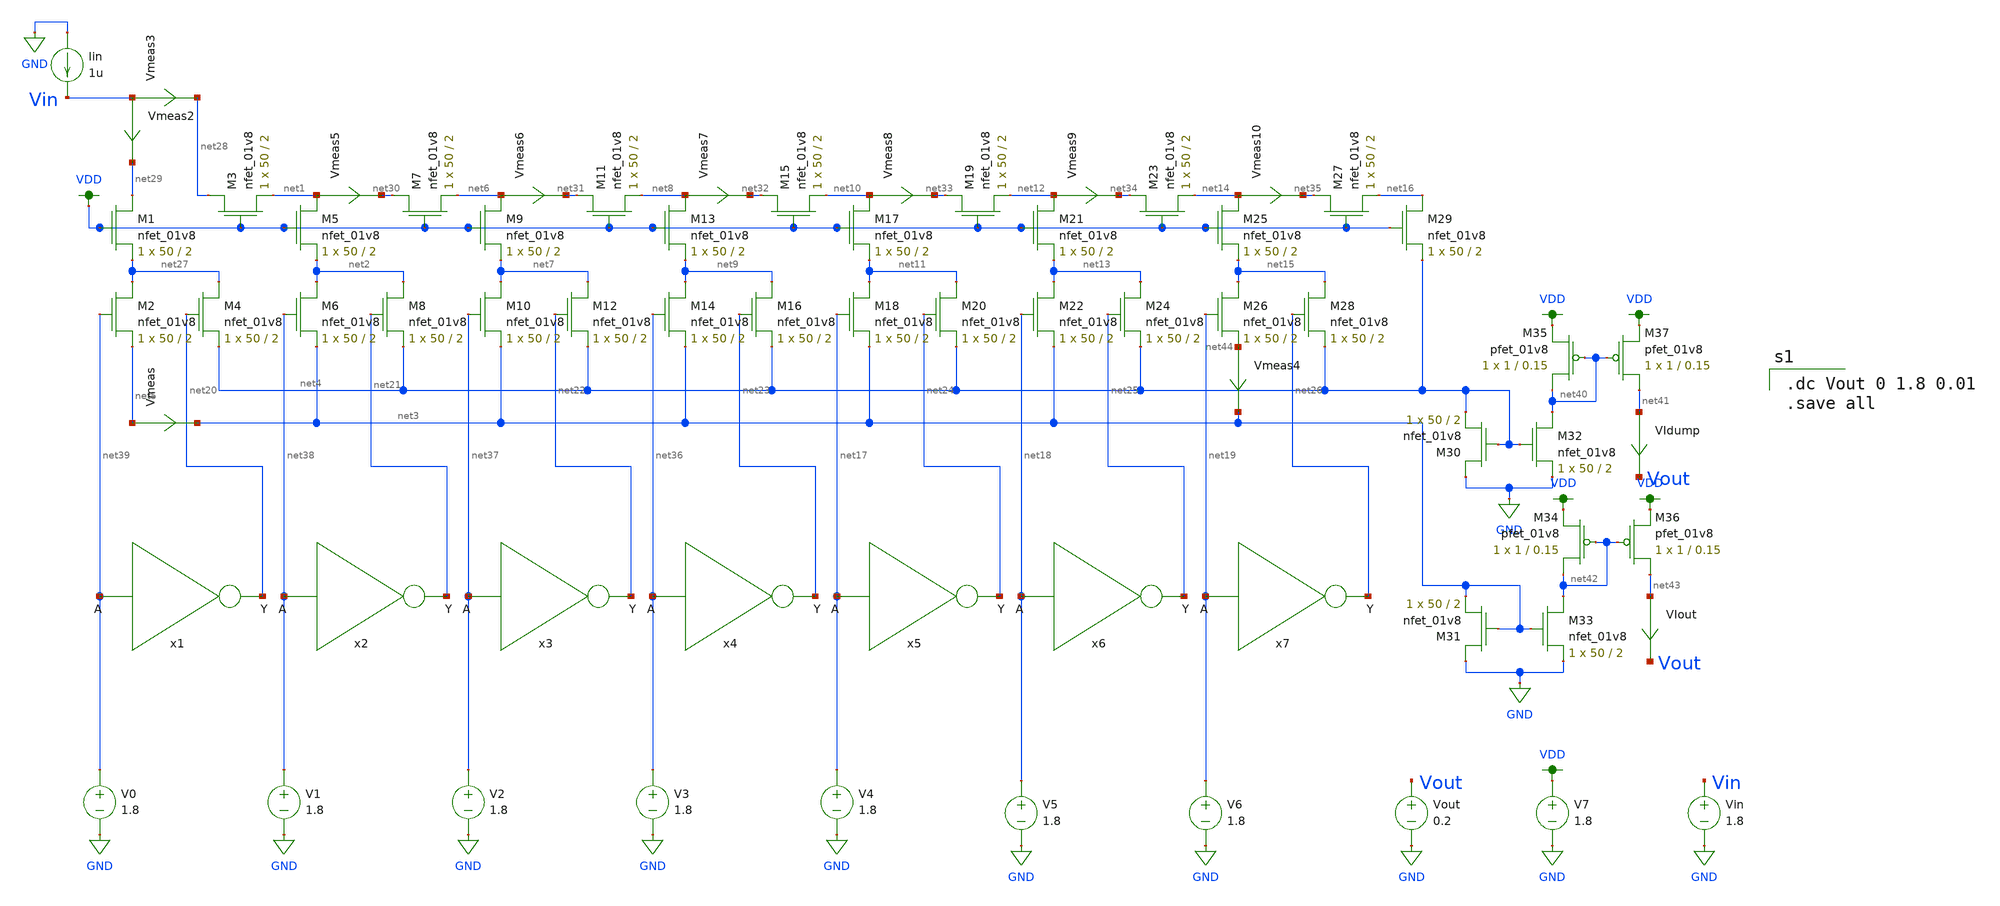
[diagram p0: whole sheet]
** sch_path: xschem/ladder_lauren.sch
**.subckt ladder_lauren
XM1 net29 VDD net27 GND sky130_fd_pr__nfet_01v8 L=2 W=50 nf=1 ad='int((nf+1)/2) * W/nf * 0.29' as='int((nf+2)/2) * W/nf * 0.29'
+ pd='2*int((nf+1)/2) * (W/nf + 0.29)' ps='2*int((nf+2)/2) * (W/nf + 0.29)' nrd='0.29 / W' nrs='0.29 / W'
+ sa=0 sb=0 sd=0 mult=1 m=1
XM3 net28 VDD net1 GND sky130_fd_pr__nfet_01v8 L=2 W=50 nf=1 ad='int((nf+1)/2) * W/nf * 0.29' as='int((nf+2)/2) * W/nf * 0.29'
+ pd='2*int((nf+1)/2) * (W/nf + 0.29)' ps='2*int((nf+2)/2) * (W/nf + 0.29)' nrd='0.29 / W' nrs='0.29 / W'
+ sa=0 sb=0 sd=0 mult=1 m=1
XM5 net1 VDD net2 GND sky130_fd_pr__nfet_01v8 L=2 W=50 nf=1 ad='int((nf+1)/2) * W/nf * 0.29' as='int((nf+2)/2) * W/nf * 0.29'
+ pd='2*int((nf+1)/2) * (W/nf + 0.29)' ps='2*int((nf+2)/2) * (W/nf + 0.29)' nrd='0.29 / W' nrs='0.29 / W'
+ sa=0 sb=0 sd=0 mult=1 m=1
XM7 net30 VDD net6 GND sky130_fd_pr__nfet_01v8 L=2 W=50 nf=1 ad='int((nf+1)/2) * W/nf * 0.29' as='int((nf+2)/2) * W/nf * 0.29'
+ pd='2*int((nf+1)/2) * (W/nf + 0.29)' ps='2*int((nf+2)/2) * (W/nf + 0.29)' nrd='0.29 / W' nrs='0.29 / W'
+ sa=0 sb=0 sd=0 mult=1 m=1
XM6 net2 net38 net3 GND sky130_fd_pr__nfet_01v8 L=2 W=50 nf=1 ad='int((nf+1)/2) * W/nf * 0.29' as='int((nf+2)/2) * W/nf * 0.29'
+ pd='2*int((nf+1)/2) * (W/nf + 0.29)' ps='2*int((nf+2)/2) * (W/nf + 0.29)' nrd='0.29 / W' nrs='0.29 / W'
+ sa=0 sb=0 sd=0 mult=1 m=1
XM8 net2 net21 net4 GND sky130_fd_pr__nfet_01v8 L=2 W=50 nf=1 ad='int((nf+1)/2) * W/nf * 0.29' as='int((nf+2)/2) * W/nf * 0.29'
+ pd='2*int((nf+1)/2) * (W/nf + 0.29)' ps='2*int((nf+2)/2) * (W/nf + 0.29)' nrd='0.29 / W' nrs='0.29 / W'
+ sa=0 sb=0 sd=0 mult=1 m=1
XM2 net27 net39 net5 GND sky130_fd_pr__nfet_01v8 L=2 W=50 nf=1 ad='int((nf+1)/2) * W/nf * 0.29' as='int((nf+2)/2) * W/nf * 0.29'
+ pd='2*int((nf+1)/2) * (W/nf + 0.29)' ps='2*int((nf+2)/2) * (W/nf + 0.29)' nrd='0.29 / W' nrs='0.29 / W'
+ sa=0 sb=0 sd=0 mult=1 m=1
XM4 net27 net20 net4 GND sky130_fd_pr__nfet_01v8 L=2 W=50 nf=1 ad='int((nf+1)/2) * W/nf * 0.29' as='int((nf+2)/2) * W/nf * 0.29'
+ pd='2*int((nf+1)/2) * (W/nf + 0.29)' ps='2*int((nf+2)/2) * (W/nf + 0.29)' nrd='0.29 / W' nrs='0.29 / W'
+ sa=0 sb=0 sd=0 mult=1 m=1
XM9 net6 VDD net7 GND sky130_fd_pr__nfet_01v8 L=2 W=50 nf=1 ad='int((nf+1)/2) * W/nf * 0.29' as='int((nf+2)/2) * W/nf * 0.29'
+ pd='2*int((nf+1)/2) * (W/nf + 0.29)' ps='2*int((nf+2)/2) * (W/nf + 0.29)' nrd='0.29 / W' nrs='0.29 / W'
+ sa=0 sb=0 sd=0 mult=1 m=1
XM11 net31 VDD net8 GND sky130_fd_pr__nfet_01v8 L=2 W=50 nf=1 ad='int((nf+1)/2) * W/nf * 0.29' as='int((nf+2)/2) * W/nf * 0.29'
+ pd='2*int((nf+1)/2) * (W/nf + 0.29)' ps='2*int((nf+2)/2) * (W/nf + 0.29)' nrd='0.29 / W' nrs='0.29 / W'
+ sa=0 sb=0 sd=0 mult=1 m=1
XM10 net7 net37 net3 GND sky130_fd_pr__nfet_01v8 L=2 W=50 nf=1 ad='int((nf+1)/2) * W/nf * 0.29' as='int((nf+2)/2) * W/nf * 0.29'
+ pd='2*int((nf+1)/2) * (W/nf + 0.29)' ps='2*int((nf+2)/2) * (W/nf + 0.29)' nrd='0.29 / W' nrs='0.29 / W'
+ sa=0 sb=0 sd=0 mult=1 m=1
XM12 net7 net22 net4 GND sky130_fd_pr__nfet_01v8 L=2 W=50 nf=1 ad='int((nf+1)/2) * W/nf * 0.29' as='int((nf+2)/2) * W/nf * 0.29'
+ pd='2*int((nf+1)/2) * (W/nf + 0.29)' ps='2*int((nf+2)/2) * (W/nf + 0.29)' nrd='0.29 / W' nrs='0.29 / W'
+ sa=0 sb=0 sd=0 mult=1 m=1
XM13 net8 VDD net9 GND sky130_fd_pr__nfet_01v8 L=2 W=50 nf=1 ad='int((nf+1)/2) * W/nf * 0.29' as='int((nf+2)/2) * W/nf * 0.29'
+ pd='2*int((nf+1)/2) * (W/nf + 0.29)' ps='2*int((nf+2)/2) * (W/nf + 0.29)' nrd='0.29 / W' nrs='0.29 / W'
+ sa=0 sb=0 sd=0 mult=1 m=1
XM15 net32 VDD net10 GND sky130_fd_pr__nfet_01v8 L=2 W=50 nf=1 ad='int((nf+1)/2) * W/nf * 0.29' as='int((nf+2)/2) * W/nf * 0.29'
+ pd='2*int((nf+1)/2) * (W/nf + 0.29)' ps='2*int((nf+2)/2) * (W/nf + 0.29)' nrd='0.29 / W' nrs='0.29 / W'
+ sa=0 sb=0 sd=0 mult=1 m=1
XM14 net9 net36 net3 GND sky130_fd_pr__nfet_01v8 L=2 W=50 nf=1 ad='int((nf+1)/2) * W/nf * 0.29' as='int((nf+2)/2) * W/nf * 0.29'
+ pd='2*int((nf+1)/2) * (W/nf + 0.29)' ps='2*int((nf+2)/2) * (W/nf + 0.29)' nrd='0.29 / W' nrs='0.29 / W'
+ sa=0 sb=0 sd=0 mult=1 m=1
XM16 net9 net23 net4 GND sky130_fd_pr__nfet_01v8 L=2 W=50 nf=1 ad='int((nf+1)/2) * W/nf * 0.29' as='int((nf+2)/2) * W/nf * 0.29'
+ pd='2*int((nf+1)/2) * (W/nf + 0.29)' ps='2*int((nf+2)/2) * (W/nf + 0.29)' nrd='0.29 / W' nrs='0.29 / W'
+ sa=0 sb=0 sd=0 mult=1 m=1
XM17 net10 VDD net11 GND sky130_fd_pr__nfet_01v8 L=2 W=50 nf=1 ad='int((nf+1)/2) * W/nf * 0.29' as='int((nf+2)/2) * W/nf * 0.29'
+ pd='2*int((nf+1)/2) * (W/nf + 0.29)' ps='2*int((nf+2)/2) * (W/nf + 0.29)' nrd='0.29 / W' nrs='0.29 / W'
+ sa=0 sb=0 sd=0 mult=1 m=1
XM19 net33 VDD net12 GND sky130_fd_pr__nfet_01v8 L=2 W=50 nf=1 ad='int((nf+1)/2) * W/nf * 0.29' as='int((nf+2)/2) * W/nf * 0.29'
+ pd='2*int((nf+1)/2) * (W/nf + 0.29)' ps='2*int((nf+2)/2) * (W/nf + 0.29)' nrd='0.29 / W' nrs='0.29 / W'
+ sa=0 sb=0 sd=0 mult=1 m=1
XM18 net11 net17 net3 GND sky130_fd_pr__nfet_01v8 L=2 W=50 nf=1 ad='int((nf+1)/2) * W/nf * 0.29' as='int((nf+2)/2) * W/nf * 0.29'
+ pd='2*int((nf+1)/2) * (W/nf + 0.29)' ps='2*int((nf+2)/2) * (W/nf + 0.29)' nrd='0.29 / W' nrs='0.29 / W'
+ sa=0 sb=0 sd=0 mult=1 m=1
XM20 net11 net24 net4 GND sky130_fd_pr__nfet_01v8 L=2 W=50 nf=1 ad='int((nf+1)/2) * W/nf * 0.29' as='int((nf+2)/2) * W/nf * 0.29'
+ pd='2*int((nf+1)/2) * (W/nf + 0.29)' ps='2*int((nf+2)/2) * (W/nf + 0.29)' nrd='0.29 / W' nrs='0.29 / W'
+ sa=0 sb=0 sd=0 mult=1 m=1
XM21 net12 VDD net13 GND sky130_fd_pr__nfet_01v8 L=2 W=50 nf=1 ad='int((nf+1)/2) * W/nf * 0.29' as='int((nf+2)/2) * W/nf * 0.29'
+ pd='2*int((nf+1)/2) * (W/nf + 0.29)' ps='2*int((nf+2)/2) * (W/nf + 0.29)' nrd='0.29 / W' nrs='0.29 / W'
+ sa=0 sb=0 sd=0 mult=1 m=1
XM23 net34 VDD net14 GND sky130_fd_pr__nfet_01v8 L=2 W=50 nf=1 ad='int((nf+1)/2) * W/nf * 0.29' as='int((nf+2)/2) * W/nf * 0.29'
+ pd='2*int((nf+1)/2) * (W/nf + 0.29)' ps='2*int((nf+2)/2) * (W/nf + 0.29)' nrd='0.29 / W' nrs='0.29 / W'
+ sa=0 sb=0 sd=0 mult=1 m=1
XM22 net13 net18 net3 GND sky130_fd_pr__nfet_01v8 L=2 W=50 nf=1 ad='int((nf+1)/2) * W/nf * 0.29' as='int((nf+2)/2) * W/nf * 0.29'
+ pd='2*int((nf+1)/2) * (W/nf + 0.29)' ps='2*int((nf+2)/2) * (W/nf + 0.29)' nrd='0.29 / W' nrs='0.29 / W'
+ sa=0 sb=0 sd=0 mult=1 m=1
XM24 net13 net25 net4 GND sky130_fd_pr__nfet_01v8 L=2 W=50 nf=1 ad='int((nf+1)/2) * W/nf * 0.29' as='int((nf+2)/2) * W/nf * 0.29'
+ pd='2*int((nf+1)/2) * (W/nf + 0.29)' ps='2*int((nf+2)/2) * (W/nf + 0.29)' nrd='0.29 / W' nrs='0.29 / W'
+ sa=0 sb=0 sd=0 mult=1 m=1
XM25 net14 VDD net15 GND sky130_fd_pr__nfet_01v8 L=2 W=50 nf=1 ad='int((nf+1)/2) * W/nf * 0.29' as='int((nf+2)/2) * W/nf * 0.29'
+ pd='2*int((nf+1)/2) * (W/nf + 0.29)' ps='2*int((nf+2)/2) * (W/nf + 0.29)' nrd='0.29 / W' nrs='0.29 / W'
+ sa=0 sb=0 sd=0 mult=1 m=1
XM27 net35 VDD net16 GND sky130_fd_pr__nfet_01v8 L=2 W=50 nf=1 ad='int((nf+1)/2) * W/nf * 0.29' as='int((nf+2)/2) * W/nf * 0.29'
+ pd='2*int((nf+1)/2) * (W/nf + 0.29)' ps='2*int((nf+2)/2) * (W/nf + 0.29)' nrd='0.29 / W' nrs='0.29 / W'
+ sa=0 sb=0 sd=0 mult=1 m=1
XM26 net15 net19 net44 GND sky130_fd_pr__nfet_01v8 L=2 W=50 nf=1 ad='int((nf+1)/2) * W/nf * 0.29' as='int((nf+2)/2) * W/nf * 0.29'
+ pd='2*int((nf+1)/2) * (W/nf + 0.29)' ps='2*int((nf+2)/2) * (W/nf + 0.29)' nrd='0.29 / W' nrs='0.29 / W'
+ sa=0 sb=0 sd=0 mult=1 m=1
XM28 net15 net26 net4 GND sky130_fd_pr__nfet_01v8 L=2 W=50 nf=1 ad='int((nf+1)/2) * W/nf * 0.29' as='int((nf+2)/2) * W/nf * 0.29'
+ pd='2*int((nf+1)/2) * (W/nf + 0.29)' ps='2*int((nf+2)/2) * (W/nf + 0.29)' nrd='0.29 / W' nrs='0.29 / W'
+ sa=0 sb=0 sd=0 mult=1 m=1
XM29 net16 VDD net4 GND sky130_fd_pr__nfet_01v8 L=2 W=50 nf=1 ad='int((nf+1)/2) * W/nf * 0.29' as='int((nf+2)/2) * W/nf * 0.29'
+ pd='2*int((nf+1)/2) * (W/nf + 0.29)' ps='2*int((nf+2)/2) * (W/nf + 0.29)' nrd='0.29 / W' nrs='0.29 / W'
+ sa=0 sb=0 sd=0 mult=1 m=1
XM30 GND net4 net4 GND sky130_fd_pr__nfet_01v8 L=2 W=50 nf=1 ad='int((nf+1)/2) * W/nf * 0.29' as='int((nf+2)/2) * W/nf * 0.29'
+ pd='2*int((nf+1)/2) * (W/nf + 0.29)' ps='2*int((nf+2)/2) * (W/nf + 0.29)' nrd='0.29 / W' nrs='0.29 / W'
+ sa=0 sb=0 sd=0 mult=1 m=1
XM31 GND net3 net3 GND sky130_fd_pr__nfet_01v8 L=2 W=50 nf=1 ad='int((nf+1)/2) * W/nf * 0.29' as='int((nf+2)/2) * W/nf * 0.29'
+ pd='2*int((nf+1)/2) * (W/nf + 0.29)' ps='2*int((nf+2)/2) * (W/nf + 0.29)' nrd='0.29 / W' nrs='0.29 / W'
+ sa=0 sb=0 sd=0 mult=1 m=1
XM32 net40 net4 GND GND sky130_fd_pr__nfet_01v8 L=2 W=50 nf=1 ad='int((nf+1)/2) * W/nf * 0.29' as='int((nf+2)/2) * W/nf * 0.29'
+ pd='2*int((nf+1)/2) * (W/nf + 0.29)' ps='2*int((nf+2)/2) * (W/nf + 0.29)' nrd='0.29 / W' nrs='0.29 / W'
+ sa=0 sb=0 sd=0 mult=1 m=1
XM33 net42 net3 GND GND sky130_fd_pr__nfet_01v8 L=2 W=50 nf=1 ad='int((nf+1)/2) * W/nf * 0.29' as='int((nf+2)/2) * W/nf * 0.29'
+ pd='2*int((nf+1)/2) * (W/nf + 0.29)' ps='2*int((nf+2)/2) * (W/nf + 0.29)' nrd='0.29 / W' nrs='0.29 / W'
+ sa=0 sb=0 sd=0 mult=1 m=1
x1 net20 net39 inverter
x2 net21 net38 inverter
x3 net22 net37 inverter
x4 net23 net36 inverter
x5 net24 net17 inverter
x6 net25 net18 inverter
x7 net26 net19 inverter
Iin GND Vin 1u
V0 net39 GND 1.8
V1 net38 GND 1.8
V2 net37 GND 1.8
V3 net36 GND 1.8
V4 net17 GND 1.8
V5 net18 GND 1.8
V6 net19 GND 1.8
VIout net43 Vout 0
.save i(viout)
VIdump net41 Vout 0
.save i(vidump)
Vout Vout GND 0.2
Vmeas net5 net3 0
.save i(vmeas)
Vmeas3 Vin net28 0
.save i(vmeas3)
Vmeas4 net44 net3 0
.save i(vmeas4)
Vmeas5 net1 net30 0
.save i(vmeas5)
Vmeas6 net6 net31 0
.save i(vmeas6)
Vmeas7 net8 net32 0
.save i(vmeas7)
Vin Vin GND 1.8
Vmeas2 Vin net29 0
.save i(vmeas2)
Vmeas8 net10 net33 0
.save i(vmeas8)
Vmeas9 net12 net34 0
.save i(vmeas9)
Vmeas10 net14 net35 0
.save i(vmeas10)
XM35 net40 net40 VDD VDD sky130_fd_pr__pfet_01v8 L=0.15 W=1 nf=1 ad='int((nf+1)/2) * W/nf * 0.29' as='int((nf+2)/2) * W/nf * 0.29'
+ pd='2*int((nf+1)/2) * (W/nf + 0.29)' ps='2*int((nf+2)/2) * (W/nf + 0.29)' nrd='0.29 / W' nrs='0.29 / W'
+ sa=0 sb=0 sd=0 mult=1 m=1
XM37 net41 net40 VDD VDD sky130_fd_pr__pfet_01v8 L=0.15 W=1 nf=1 ad='int((nf+1)/2) * W/nf * 0.29' as='int((nf+2)/2) * W/nf * 0.29'
+ pd='2*int((nf+1)/2) * (W/nf + 0.29)' ps='2*int((nf+2)/2) * (W/nf + 0.29)' nrd='0.29 / W' nrs='0.29 / W'
+ sa=0 sb=0 sd=0 mult=1 m=1
XM34 net42 net42 VDD VDD sky130_fd_pr__pfet_01v8 L=0.15 W=1 nf=1 ad='int((nf+1)/2) * W/nf * 0.29' as='int((nf+2)/2) * W/nf * 0.29'
+ pd='2*int((nf+1)/2) * (W/nf + 0.29)' ps='2*int((nf+2)/2) * (W/nf + 0.29)' nrd='0.29 / W' nrs='0.29 / W'
+ sa=0 sb=0 sd=0 mult=1 m=1
XM36 net43 net42 VDD VDD sky130_fd_pr__pfet_01v8 L=0.15 W=1 nf=1 ad='int((nf+1)/2) * W/nf * 0.29' as='int((nf+2)/2) * W/nf * 0.29'
+ pd='2*int((nf+1)/2) * (W/nf + 0.29)' ps='2*int((nf+2)/2) * (W/nf + 0.29)' nrd='0.29 / W' nrs='0.29 / W'
+ sa=0 sb=0 sd=0 mult=1 m=1
V7 VDD GND 1.8
**** begin user architecture code

.option wnflag=1
.lib ~/skywater/skywater-pdk/libraries/sky130_fd_pr_ngspice/latest/models/sky130.lib.spice tt


.dc Vout 0 1.8 0.01
.save all

**** end user architecture code
**.ends

* expanding   symbol:  ./inverter.sym # of pins=2
** sym_path: xschem/inverter.sym
** sch_path: xschem/inverter.sch
.subckt inverter Y A
*.ipin A
*.opin Y
XM1 Y A VDD VDD sky130_fd_pr__pfet_01v8 L=0.15 W=1 nf=1 ad='int((nf+1)/2) * W/nf * 0.29' as='int((nf+2)/2) * W/nf * 0.29'
+ pd='2*int((nf+1)/2) * (W/nf + 0.29)' ps='2*int((nf+2)/2) * (W/nf + 0.29)' nrd='0.29 / W' nrs='0.29 / W'
+ sa=0 sb=0 sd=0 mult=1 m=1
XM2 Y A GND GND sky130_fd_pr__nfet_01v8 L=0.15 W=1 nf=1 ad='int((nf+1)/2) * W/nf * 0.29' as='int((nf+2)/2) * W/nf * 0.29'
+ pd='2*int((nf+1)/2) * (W/nf + 0.29)' ps='2*int((nf+2)/2) * (W/nf + 0.29)' nrd='0.29 / W' nrs='0.29 / W'
+ sa=0 sb=0 sd=0 mult=1 m=1
.ends

.GLOBAL VDD
.GLOBAL GND
.end
